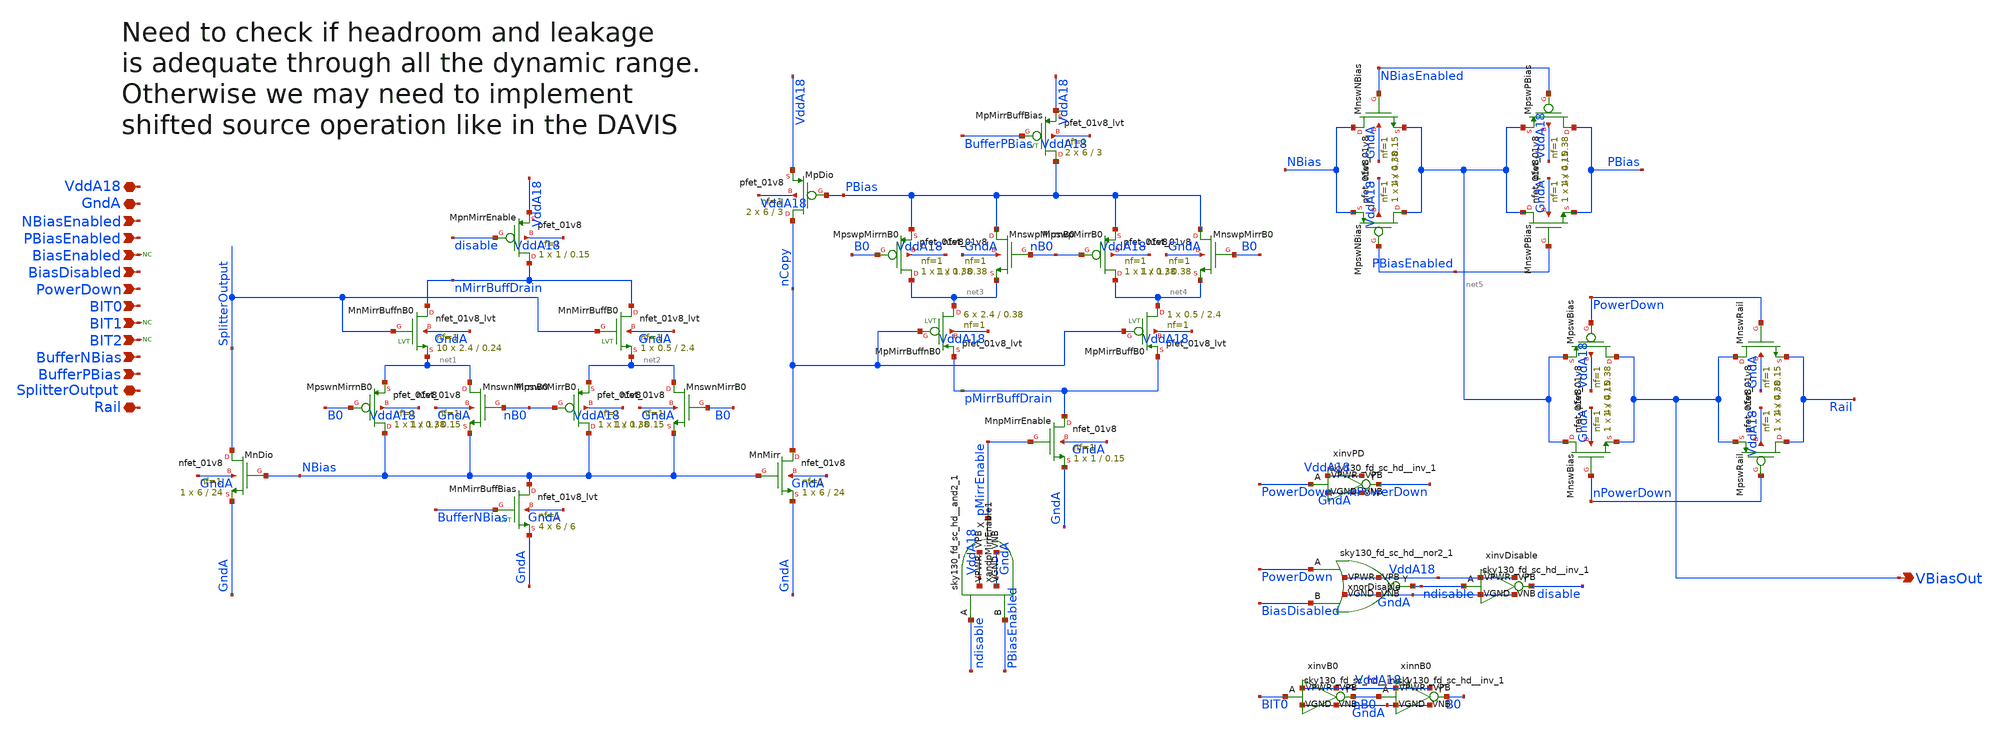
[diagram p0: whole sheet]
** sch_path: analog/xschem/BiasBuffers.sch
**.subckt BiasBuffers GndA VddA18 VBiasOut NBiasEnabled PBiasEnabled BiasEnabled BiasDisabled
*+ PowerDown BIT0 BIT1 BIT2 BufferNBias BufferPBias SplitterOutput Rail
*.iopin GndA
*.iopin VddA18
*.opin VBiasOut
*.ipin NBiasEnabled
*.ipin PBiasEnabled
*.ipin BiasEnabled
*.ipin BiasDisabled
*.ipin PowerDown
*.ipin BIT0
*.ipin BIT1
*.ipin BIT2
*.ipin BufferNBias
*.ipin BufferPBias
*.iopin SplitterOutput
*.iopin Rail
XMnDio SplitterOutput NBias GndA GndA sky130_fd_pr__nfet_01v8 L=24 W=6 nf=1 ad='int((1 + 1)/2) * 6 / 1 * 0.29'
+ as='int((1 + 2)/2) * 6 / 1 * 0.29' pd='2*int((1 + 1)/2) * (6 / 1 + 0.29)' ps='2*int((1 + 2)/2) * (6 / 1 + 0.29)'
+ nrd='0.29 / 6 ' nrs='0.29 / 6 ' sa=0 sb=0 sd=0 mult=1 m=1
XMnswnMirrnB0 net1 nB0 NBias GndA sky130_fd_pr__nfet_01v8 L=0.15 W=1 nf=1 ad='int((1 + 1)/2) * 1 / 1 * 0.29'
+ as='int((1 + 2)/2) * 1 / 1 * 0.29' pd='2*int((1 + 1)/2) * (1 / 1 + 0.29)' ps='2*int((1 + 2)/2) * (1 / 1 + 0.29)'
+ nrd='0.29 / 1 ' nrs='0.29 / 1 ' sa=0 sb=0 sd=0 mult=1 m=1
XMpswnMirrnB0 NBias B0 net1 VddA18 sky130_fd_pr__pfet_01v8 L=0.38 W=1 nf=1 ad='int((1 + 1)/2) * 1 / 1 * 0.29'
+ as='int((1 + 2)/2) * 1 / 1 * 0.29' pd='2*int((1 + 1)/2) * (1 / 1 + 0.29)' ps='2*int((1 + 2)/2) * (1 / 1 + 0.29)'
+ nrd='0.29 / 1 ' nrs='0.29 / 1 ' sa=0 sb=0 sd=0 mult=1 m=1
XMnMirrBuffB0 nMirrBuffDrain SplitterOutput net2 GndA sky130_fd_pr__nfet_01v8_lvt L=2.4 W=0.5 nf=1 ad='int((1 + 1)/2) * 0.5 / 1 * 0.29'
+ as='int((1 + 2)/2) * 0.5 / 1 * 0.29' pd='2*int((1 + 1)/2) * (0.5 / 1 + 0.29)' ps='2*int((1 + 2)/2) * (0.5 / 1 + 0.29)'
+ nrd='0.29 / 0.5 ' nrs='0.29 / 0.5 ' sa=0 sb=0 sd=0 mult=1 m=1
XMpnMirrEnable nMirrBuffDrain disable VddA18 VddA18 sky130_fd_pr__pfet_01v8 L=0.15 W=1 nf=1 ad='int((1 + 1)/2) * 1 / 1 * 0.29'
+ as='int((1 + 2)/2) * 1 / 1 * 0.29' pd='2*int((1 + 1)/2) * (1 / 1 + 0.29)' ps='2*int((1 + 2)/2) * (1 / 1 + 0.29)'
+ nrd='0.29 / 1 ' nrs='0.29 / 1 ' sa=0 sb=0 sd=0 mult=1 m=1
XMnswnMirrB0 net2 B0 NBias GndA sky130_fd_pr__nfet_01v8 L=0.15 W=1 nf=1 ad='int((1 + 1)/2) * 1 / 1 * 0.29'
+ as='int((1 + 2)/2) * 1 / 1 * 0.29' pd='2*int((1 + 1)/2) * (1 / 1 + 0.29)' ps='2*int((1 + 2)/2) * (1 / 1 + 0.29)'
+ nrd='0.29 / 1 ' nrs='0.29 / 1 ' sa=0 sb=0 sd=0 mult=1 m=1
XMpswnMirrB0 NBias nB0 net2 VddA18 sky130_fd_pr__pfet_01v8 L=0.38 W=1 nf=1 ad='int((1 + 1)/2) * 1 / 1 * 0.29'
+ as='int((1 + 2)/2) * 1 / 1 * 0.29' pd='2*int((1 + 1)/2) * (1 / 1 + 0.29)' ps='2*int((1 + 2)/2) * (1 / 1 + 0.29)'
+ nrd='0.29 / 1 ' nrs='0.29 / 1 ' sa=0 sb=0 sd=0 mult=1 m=1
XMnMirr nCopy NBias GndA GndA sky130_fd_pr__nfet_01v8 L=24 W=6 nf=1 ad='int((1 + 1)/2) * 6 / 1 * 0.29'
+ as='int((1 + 2)/2) * 6 / 1 * 0.29' pd='2*int((1 + 1)/2) * (6 / 1 + 0.29)' ps='2*int((1 + 2)/2) * (6 / 1 + 0.29)'
+ nrd='0.29 / 6 ' nrs='0.29 / 6 ' sa=0 sb=0 sd=0 mult=1 m=1
XMnMirrBuffBias NBias BufferNBias GndA GndA sky130_fd_pr__nfet_01v8_lvt L=6 W=6 nf=1 ad='int((1 + 1)/2) * 6 / 1 * 0.29'
+ as='int((1 + 2)/2) * 6 / 1 * 0.29' pd='2*int((1 + 1)/2) * (6 / 1 + 0.29)' ps='2*int((1 + 2)/2) * (6 / 1 + 0.29)'
+ nrd='0.29 / 6 ' nrs='0.29 / 6 ' sa=0 sb=0 sd=0 mult=4 m=4
XMpDio nCopy PBias VddA18 VddA18 sky130_fd_pr__pfet_01v8 L=3 W=6 nf=1 ad='int((1 + 1)/2) * 6 / 1 * 0.29'
+ as='int((1 + 2)/2) * 6 / 1 * 0.29' pd='2*int((1 + 1)/2) * (6 / 1 + 0.29)' ps='2*int((1 + 2)/2) * (6 / 1 + 0.29)'
+ nrd='0.29 / 6 ' nrs='0.29 / 6 ' sa=0 sb=0 sd=0 mult=2 m=2
XMnswpMirrnB0 PBias nB0 net3 GndA sky130_fd_pr__nfet_01v8 L=0.38 W=1 nf=1 ad='int((1 + 1)/2) * 1 / 1 * 0.29'
+ as='int((1 + 2)/2) * 1 / 1 * 0.29' pd='2*int((1 + 1)/2) * (1 / 1 + 0.29)' ps='2*int((1 + 2)/2) * (1 / 1 + 0.29)'
+ nrd='0.29 / 1 ' nrs='0.29 / 1 ' sa=0 sb=0 sd=0 mult=1 m=1
XMpswpMirrnB0 net3 B0 PBias VddA18 sky130_fd_pr__pfet_01v8 L=0.38 W=1 nf=1 ad='int((1 + 1)/2) * 1 / 1 * 0.29'
+ as='int((1 + 2)/2) * 1 / 1 * 0.29' pd='2*int((1 + 1)/2) * (1 / 1 + 0.29)' ps='2*int((1 + 2)/2) * (1 / 1 + 0.29)'
+ nrd='0.29 / 1 ' nrs='0.29 / 1 ' sa=0 sb=0 sd=0 mult=1 m=1
XMnswpMirrB0 PBias B0 net4 GndA sky130_fd_pr__nfet_01v8 L=0.38 W=1 nf=1 ad='int((1 + 1)/2) * 1 / 1 * 0.29'
+ as='int((1 + 2)/2) * 1 / 1 * 0.29' pd='2*int((1 + 1)/2) * (1 / 1 + 0.29)' ps='2*int((1 + 2)/2) * (1 / 1 + 0.29)'
+ nrd='0.29 / 1 ' nrs='0.29 / 1 ' sa=0 sb=0 sd=0 mult=1 m=1
XMpswpMirrB0 net4 nB0 PBias VddA18 sky130_fd_pr__pfet_01v8 L=0.38 W=1 nf=1 ad='int((1 + 1)/2) * 1 / 1 * 0.29'
+ as='int((1 + 2)/2) * 1 / 1 * 0.29' pd='2*int((1 + 1)/2) * (1 / 1 + 0.29)' ps='2*int((1 + 2)/2) * (1 / 1 + 0.29)'
+ nrd='0.29 / 1 ' nrs='0.29 / 1 ' sa=0 sb=0 sd=0 mult=1 m=1
XMpMirrBuffnB0 net3 nCopy pMirrBuffDrain VddA18 sky130_fd_pr__pfet_01v8_lvt L=0.38 W=2.4 nf=1 ad='int((1 + 1)/2) * 2.4 / 1 * 0.29'
+ as='int((1 + 2)/2) * 2.4 / 1 * 0.29' pd='2*int((1 + 1)/2) * (2.4 / 1 + 0.29)' ps='2*int((1 + 2)/2) * (2.4 / 1 + 0.29)'
+ nrd='0.29 / 2.4 ' nrs='0.29 / 2.4 ' sa=0 sb=0 sd=0 mult=6 m=6
XMpMirrBuffB0 net4 nCopy pMirrBuffDrain VddA18 sky130_fd_pr__pfet_01v8_lvt L=2.4 W=0.5 nf=1 ad='int((1 + 1)/2) * 0.5 / 1 * 0.29'
+ as='int((1 + 2)/2) * 0.5 / 1 * 0.29' pd='2*int((1 + 1)/2) * (0.5 / 1 + 0.29)' ps='2*int((1 + 2)/2) * (0.5 / 1 + 0.29)'
+ nrd='0.29 / 0.5 ' nrs='0.29 / 0.5 ' sa=0 sb=0 sd=0 mult=1 m=1
XMnpMirrEnable pMirrBuffDrain pMirrEnable GndA GndA sky130_fd_pr__nfet_01v8 L=0.15 W=1 nf=1 ad='int((1 + 1)/2) * 1 / 1 * 0.29'
+ as='int((1 + 2)/2) * 1 / 1 * 0.29' pd='2*int((1 + 1)/2) * (1 / 1 + 0.29)' ps='2*int((1 + 2)/2) * (1 / 1 + 0.29)'
+ nrd='0.29 / 1 ' nrs='0.29 / 1 ' sa=0 sb=0 sd=0 mult=1 m=1
XMpMirrBuffBias PBias BufferPBias VddA18 VddA18 sky130_fd_pr__pfet_01v8_lvt L=3 W=6 nf=1 ad='int((1 + 1)/2) * 6 / 1 * 0.29'
+ as='int((1 + 2)/2) * 6 / 1 * 0.29' pd='2*int((1 + 1)/2) * (6 / 1 + 0.29)' ps='2*int((1 + 2)/2) * (6 / 1 + 0.29)'
+ nrd='0.29 / 6 ' nrs='0.29 / 6 ' sa=0 sb=0 sd=0 mult=2 m=2
XMnswNBias NBias NBiasEnabled net5 GndA sky130_fd_pr__nfet_01v8 L=0.15 W=4 nf=1 ad='int((1 + 1)/2) * 4 / 1 * 0.29'
+ as='int((1 + 2)/2) * 4 / 1 * 0.29' pd='2*int((1 + 1)/2) * (4 / 1 + 0.29)' ps='2*int((1 + 2)/2) * (4 / 1 + 0.29)'
+ nrd='0.29 / 4 ' nrs='0.29 / 4 ' sa=0 sb=0 sd=0 mult=1 m=1
XMpswNBias net5 PBiasEnabled NBias VddA18 sky130_fd_pr__pfet_01v8 L=0.38 W=4 nf=1 ad='int((1 + 1)/2) * 4 / 1 * 0.29'
+ as='int((1 + 2)/2) * 4 / 1 * 0.29' pd='2*int((1 + 1)/2) * (4 / 1 + 0.29)' ps='2*int((1 + 2)/2) * (4 / 1 + 0.29)'
+ nrd='0.29 / 4 ' nrs='0.29 / 4 ' sa=0 sb=0 sd=0 mult=1 m=1
XMnswPBias net5 PBiasEnabled PBias GndA sky130_fd_pr__nfet_01v8 L=0.15 W=4 nf=1 ad='int((1 + 1)/2) * 4 / 1 * 0.29'
+ as='int((1 + 2)/2) * 4 / 1 * 0.29' pd='2*int((1 + 1)/2) * (4 / 1 + 0.29)' ps='2*int((1 + 2)/2) * (4 / 1 + 0.29)'
+ nrd='0.29 / 4 ' nrs='0.29 / 4 ' sa=0 sb=0 sd=0 mult=1 m=1
XMpswPBias PBias NBiasEnabled net5 VddA18 sky130_fd_pr__pfet_01v8 L=0.38 W=4 nf=1 ad='int((1 + 1)/2) * 4 / 1 * 0.29'
+ as='int((1 + 2)/2) * 4 / 1 * 0.29' pd='2*int((1 + 1)/2) * (4 / 1 + 0.29)' ps='2*int((1 + 2)/2) * (4 / 1 + 0.29)'
+ nrd='0.29 / 4 ' nrs='0.29 / 4 ' sa=0 sb=0 sd=0 mult=1 m=1
XMnswBias net5 nPowerDown VBiasOut GndA sky130_fd_pr__nfet_01v8 L=0.15 W=4 nf=1 ad='int((1 + 1)/2) * 4 / 1 * 0.29'
+ as='int((1 + 2)/2) * 4 / 1 * 0.29' pd='2*int((1 + 1)/2) * (4 / 1 + 0.29)' ps='2*int((1 + 2)/2) * (4 / 1 + 0.29)'
+ nrd='0.29 / 4 ' nrs='0.29 / 4 ' sa=0 sb=0 sd=0 mult=1 m=1
XMpswBias VBiasOut PowerDown net5 VddA18 sky130_fd_pr__pfet_01v8 L=0.38 W=4 nf=1 ad='int((1 + 1)/2) * 4 / 1 * 0.29'
+ as='int((1 + 2)/2) * 4 / 1 * 0.29' pd='2*int((1 + 1)/2) * (4 / 1 + 0.29)' ps='2*int((1 + 2)/2) * (4 / 1 + 0.29)'
+ nrd='0.29 / 4 ' nrs='0.29 / 4 ' sa=0 sb=0 sd=0 mult=1 m=1
XMnswRail VBiasOut PowerDown Rail GndA sky130_fd_pr__nfet_01v8 L=0.15 W=4 nf=1 ad='int((1 + 1)/2) * 4 / 1 * 0.29'
+ as='int((1 + 2)/2) * 4 / 1 * 0.29' pd='2*int((1 + 1)/2) * (4 / 1 + 0.29)' ps='2*int((1 + 2)/2) * (4 / 1 + 0.29)'
+ nrd='0.29 / 4 ' nrs='0.29 / 4 ' sa=0 sb=0 sd=0 mult=1 m=1
XMpswRail Rail nPowerDown VBiasOut VddA18 sky130_fd_pr__pfet_01v8 L=0.38 W=4 nf=1 ad='int((1 + 1)/2) * 4 / 1 * 0.29'
+ as='int((1 + 2)/2) * 4 / 1 * 0.29' pd='2*int((1 + 1)/2) * (4 / 1 + 0.29)' ps='2*int((1 + 2)/2) * (4 / 1 + 0.29)'
+ nrd='0.29 / 4 ' nrs='0.29 / 4 ' sa=0 sb=0 sd=0 mult=1 m=1
* noconn BiasEnabled
* noconn BIT1
* noconn BIT2
xinvB0 BIT0 nB0 VddA18 VddA18 GndA GndA sky130_fd_sc_hd__inv_1
xinnB0 nB0 B0 VddA18 VddA18 GndA GndA sky130_fd_sc_hd__inv_1
xnorDisable PowerDown BiasDisabled ndisable VddA18 VddA18 GndA GndA sky130_fd_sc_hd__nor2_1
xinvDisable ndisable disable VddA18 VddA18 GndA GndA sky130_fd_sc_hd__inv_1
xinvPD PowerDown nPowerDown VddA18 VddA18 GndA GndA sky130_fd_sc_hd__inv_1
xandpMirrEnable1 ndisable PBiasEnabled VddA18 VddA18 GndA GndA pMirrEnable sky130_fd_sc_hd__and2_1
XMnMirrBuffnB0 nMirrBuffDrain SplitterOutput net1 GndA sky130_fd_pr__nfet_01v8_lvt L=0.24 W=2.4 nf=1
+ ad='int((1 + 1)/2) * 2.4 / 1 * 0.29' as='int((1 + 2)/2) * 2.4 / 1 * 0.29' pd='2*int((1 + 1)/2) * (2.4 / 1 + 0.29)'
+ ps='2*int((1 + 2)/2) * (2.4 / 1 + 0.29)' nrd='0.29 / 2.4 ' nrs='0.29 / 2.4 ' sa=0 sb=0 sd=0 mult=10 m=10
**.ends
.end
